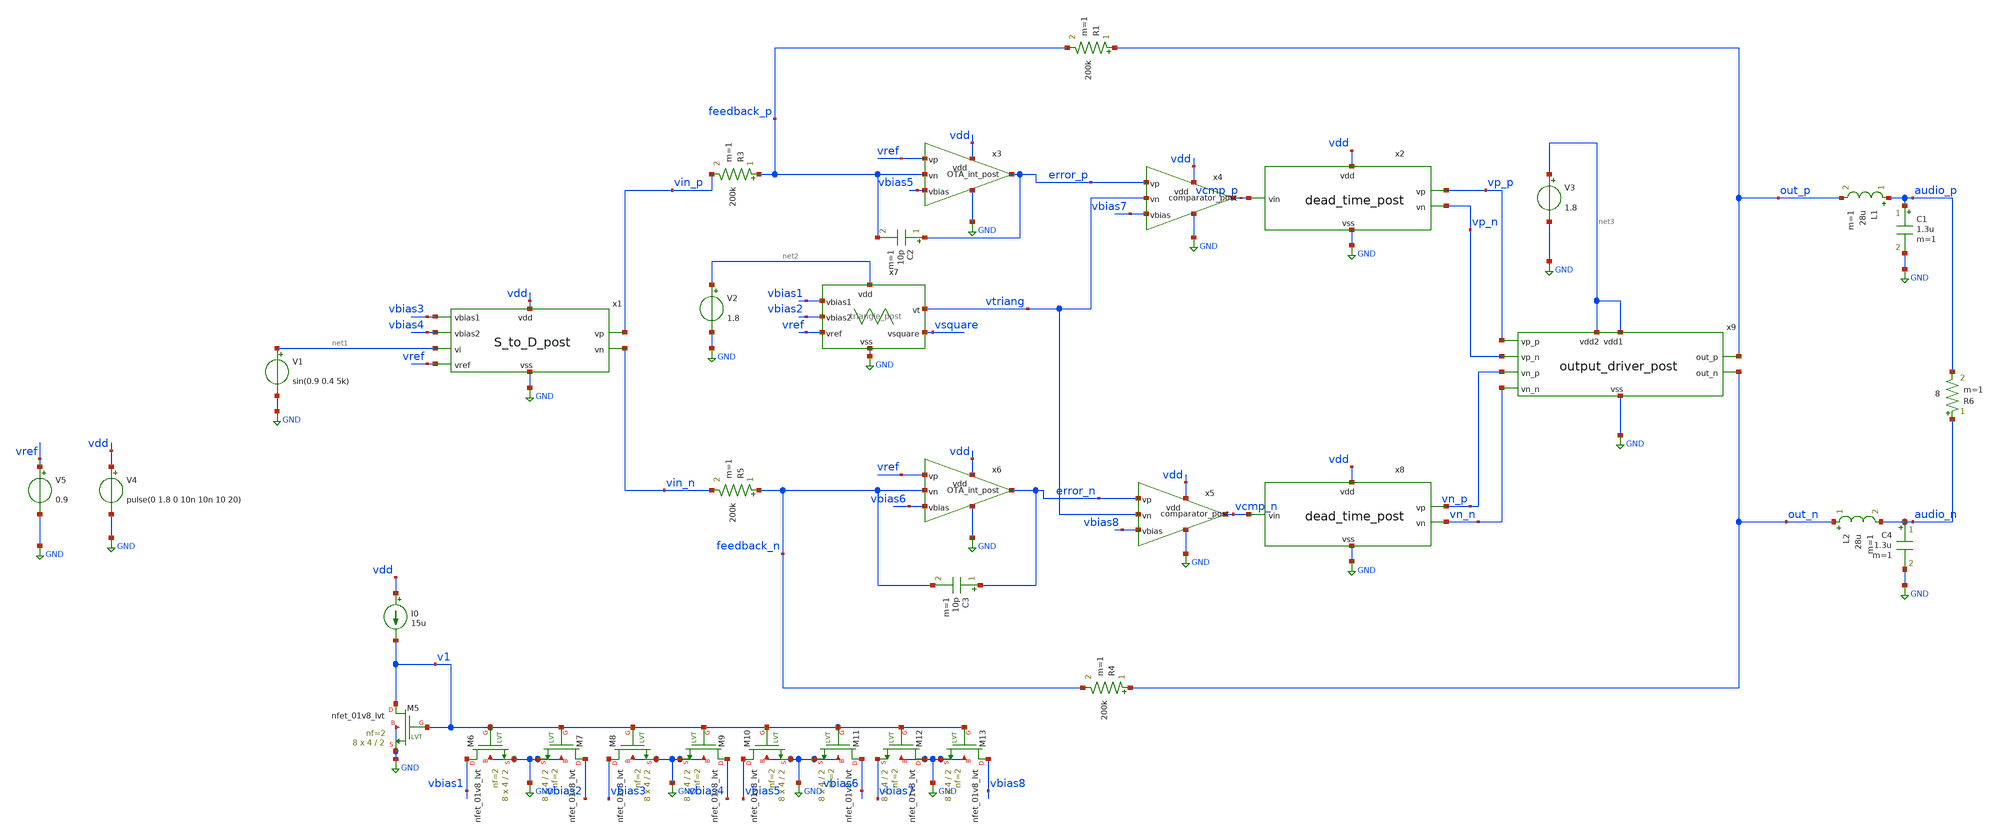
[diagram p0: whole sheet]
** sch_path: xschem/src/Class_D/Class_D_tb.sch
**.subckt Class_D_tb
V1 net1 GND sin(0.9 0.4 5k)
V5 vref GND 0.9
L1 audio_p out_p 28u m=1
C1 audio_p GND 1.3u m=1
R1 out_p feedback_p 200k m=1
R3 feedback_p vin_p 200k m=1
C2 error_p feedback_p 10p m=1
R4 out_n feedback_n 200k m=1
R5 feedback_n vin_n 200k m=1
C3 error_n feedback_n 10p m=1
L2 out_n audio_n 28u m=1
C4 audio_n GND 1.3u m=1
R6 audio_n audio_p 8 m=1
V4 vdd GND pulse(0 1.8 0 10n 10n 10 20)
I0 vdd v1 15u
XM5 v1 v1 GND GND sky130_fd_pr__nfet_01v8_lvt L=2 W=4 nf=2 ad='int((nf+1)/2) * W/nf * 0.29' as='int((nf+2)/2) * W/nf * 0.29'
+ pd='2*int((nf+1)/2) * (W/nf + 0.29)' ps='2*int((nf+2)/2) * (W/nf + 0.29)' nrd='0.29 / W' nrs='0.29 / W'
+ sa=0 sb=0 sd=0 mult=8 m=8
XM6 vbias1 v1 GND GND sky130_fd_pr__nfet_01v8_lvt L=2 W=4 nf=2 ad='int((nf+1)/2) * W/nf * 0.29' as='int((nf+2)/2) * W/nf * 0.29'
+ pd='2*int((nf+1)/2) * (W/nf + 0.29)' ps='2*int((nf+2)/2) * (W/nf + 0.29)' nrd='0.29 / W' nrs='0.29 / W'
+ sa=0 sb=0 sd=0 mult=8 m=8
XM7 vbias2 v1 GND GND sky130_fd_pr__nfet_01v8_lvt L=2 W=4 nf=2 ad='int((nf+1)/2) * W/nf * 0.29' as='int((nf+2)/2) * W/nf * 0.29'
+ pd='2*int((nf+1)/2) * (W/nf + 0.29)' ps='2*int((nf+2)/2) * (W/nf + 0.29)' nrd='0.29 / W' nrs='0.29 / W'
+ sa=0 sb=0 sd=0 mult=8 m=8
XM8 vbias3 v1 GND GND sky130_fd_pr__nfet_01v8_lvt L=2 W=4 nf=2 ad='int((nf+1)/2) * W/nf * 0.29' as='int((nf+2)/2) * W/nf * 0.29'
+ pd='2*int((nf+1)/2) * (W/nf + 0.29)' ps='2*int((nf+2)/2) * (W/nf + 0.29)' nrd='0.29 / W' nrs='0.29 / W'
+ sa=0 sb=0 sd=0 mult=8 m=8
XM9 vbias4 v1 GND GND sky130_fd_pr__nfet_01v8_lvt L=2 W=4 nf=2 ad='int((nf+1)/2) * W/nf * 0.29' as='int((nf+2)/2) * W/nf * 0.29'
+ pd='2*int((nf+1)/2) * (W/nf + 0.29)' ps='2*int((nf+2)/2) * (W/nf + 0.29)' nrd='0.29 / W' nrs='0.29 / W'
+ sa=0 sb=0 sd=0 mult=8 m=8
XM10 vbias5 v1 GND GND sky130_fd_pr__nfet_01v8_lvt L=2 W=4 nf=2 ad='int((nf+1)/2) * W/nf * 0.29' as='int((nf+2)/2) * W/nf * 0.29'
+ pd='2*int((nf+1)/2) * (W/nf + 0.29)' ps='2*int((nf+2)/2) * (W/nf + 0.29)' nrd='0.29 / W' nrs='0.29 / W'
+ sa=0 sb=0 sd=0 mult=8 m=8
XM11 vbias6 v1 GND GND sky130_fd_pr__nfet_01v8_lvt L=2 W=4 nf=2 ad='int((nf+1)/2) * W/nf * 0.29' as='int((nf+2)/2) * W/nf * 0.29'
+ pd='2*int((nf+1)/2) * (W/nf + 0.29)' ps='2*int((nf+2)/2) * (W/nf + 0.29)' nrd='0.29 / W' nrs='0.29 / W'
+ sa=0 sb=0 sd=0 mult=8 m=8
XM12 GND v1 vbias7 GND sky130_fd_pr__nfet_01v8_lvt L=2 W=4 nf=2 ad='int((nf+1)/2) * W/nf * 0.29' as='int((nf+2)/2) * W/nf * 0.29'
+ pd='2*int((nf+1)/2) * (W/nf + 0.29)' ps='2*int((nf+2)/2) * (W/nf + 0.29)' nrd='0.29 / W' nrs='0.29 / W'
+ sa=0 sb=0 sd=0 mult=8 m=8
XM13 vbias8 v1 GND GND sky130_fd_pr__nfet_01v8_lvt L=2 W=4 nf=2 ad='int((nf+1)/2) * W/nf * 0.29' as='int((nf+2)/2) * W/nf * 0.29'
+ pd='2*int((nf+1)/2) * (W/nf + 0.29)' ps='2*int((nf+2)/2) * (W/nf + 0.29)' nrd='0.29 / W' nrs='0.29 / W'
+ sa=0 sb=0 sd=0 mult=8 m=8
V2 net2 GND 1.8
x1 vdd vbias3 vbias4 net1 vref GND vin_n vin_p S_to_D_post
x7 net2 vbias1 vbias2 vref GND vsquare vtriang triangle_post
x4 vdd error_p vtriang vbias7 GND vcmp_p comparator_post
x5 vdd error_n vtriang vbias8 GND vcmp_n comparator_post
x2 vdd vcmp_p vp_p vp_n GND dead_time_post
x8 vdd vcmp_n vn_p vn_n GND dead_time_post
x9 net3 vp_p out_p GND vp_n vn_p out_n vn_n net3 output_driver_post
V3 net3 GND 1.8
x3 vdd vref feedback_p vbias5 GND error_p OTA_int_post
x6 vdd vref feedback_n vbias6 GND error_n OTA_int_post
**** begin user architecture code


.option rshunt=1e20
.nodeset V(audio_p)=0.9 V(audio_n)=0.9 V(vp_p)=0.79 V(vn_p)=0 V(vcmp_p)=0.859  V(vp_n)=0.79
+ V(vn_n)=0 V(vcmp_n)=0.859 v(vin_p)=0.9 v(vin_n)=0.9 v(vtriang)=0.9
*.nodeset all=0.9
.option VNTOL=1e-6 ABSTOL=1e-9
*.option savecurrents
*set the absolute voltage error tolerance and absolute current error tolerance
.control
save out_p out_n audio_p audio_n I(V4) I(V2) @r6[i] @r1[i] i(v3) i(v6) vtriang vin_p vin_n error_p
+ error_n vcmp_p vcmp_n vp_p vp_n vn_p vn_n
*save vtriang audio_p audio_n I(V2) @r6[i] out_p out_n
*op
tran 3n 2m 0.1m
*linearize V(audio)
*linearize V(out)
*fft V(out)
*fft V(audio)
*plot mag(V(audio))
*plot mag(V(out))
let pout=@r6[i]*(V(audio_p)-V(audio_n))
let pin=1.8*(I(V4)+I(V2)+I(V3))
meas tran pload avg pout from=4m to=9m
meas tran p_supply avg pin from=4m to=9m
*print pload/p_supply
set nfreqs=20
*fourier 10k V(out_p)-V(out_n)

fourier 5k V(audio_p)-V(audio_n)
write class_d_5k_04_post.raw

.endc





.include /home/eda/pdk/skywater-pdk/libraries/sky130_fd_pr_ngspice/latest/models/corners/tt.spice
.include /home/eda/magic/class_d_audio_amplifier/OTA/OTA_int_post.spice
.include /home/eda/magic/class_d_audio_amplifier/OTA/OTA_post.spice
.include /home/eda/magic/class_d_audio_amplifier/S_to_D/S_to_D_post.spice
.include /home/eda/magic/class_d_audio_amplifier/triang/triangle_post.spice
.include /home/eda/magic/class_d_audio_amplifier/comparator/comparator_post.spice
.include /home/eda/magic/class_d_audio_amplifier/dead_time/dead_time_post.spice
.include /home/eda/magic/class_d_audio_amplifier/output_driver/output_driver_post.spice
* Resistor$::SKYWATER_MODELS/Capacitor
.include $::SKYWATER_MODELS/models/r+c/res_typical__cap_typical.spice
.include $::SKYWATER_MODELS/models/r+c/res_typical__cap_typical__lin.spice
* Special cells
.include $::SKYWATER_MODELS/models/corners/tt/specialized_cells.spice


**** end user architecture code
**.ends
.GLOBAL GND
.end
